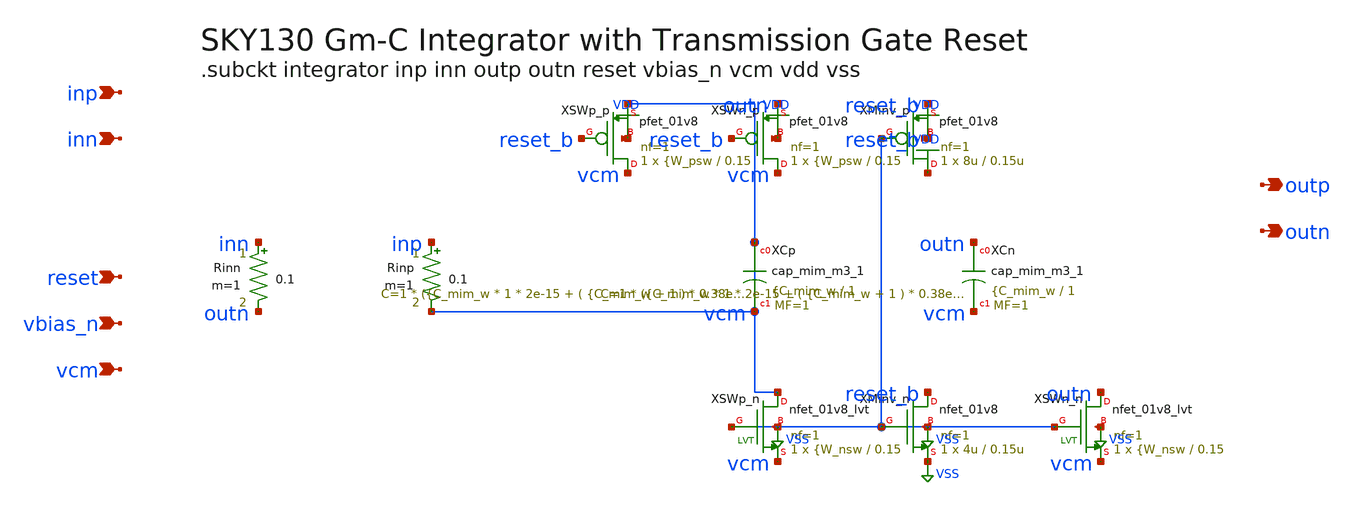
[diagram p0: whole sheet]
** sch_path: data/sch/ode_integrator.sch
**.subckt ode_integrator inp inn outp outn reset vbias_n vcm
*.ipin inp
*.ipin inn
*.opin outp
*.opin outn
*.ipin reset
*.ipin vbias_n
*.ipin vcm
XXMinv_n reset_b VSS VSS VSS sky130_fd_pr__nfet_01v8 L=0.15u W=4u nf=1 ad='int((1 + 1)/2) * 4u / 1 * 0.29'
+ as='int((1 + 2)/2) * 4u / 1 * 0.29' pd='2*int((1 + 1)/2) * (4u / 1 + 0.29)' ps='2*int((1 + 2)/2) * (4u / 1 + 0.29)'
+ nrd='0.29 / 4u ' nrs='0.29 / 4u ' sa=0 sb=0 sd=0 mult=1 m=1
XXMinv_p VDD VSS reset_b VDD sky130_fd_pr__pfet_01v8 L=0.15u W=8u nf=1 ad='int((nf+1)/2) * W/nf * 0.29'
+ as='int((nf+2)/2) * W/nf * 0.29' pd='2*int((nf+1)/2) * (W/nf + 0.29)' ps='2*int((nf+2)/2) * (W/nf + 0.29)'
+ nrd='0.29 / W' nrs='0.29 / W' sa=0 sb=0 sd=0 mult=1 m=1
XXCp vcm vcm sky130_fd_pr__cap_mim_m3_1 W={C_mim_w L=1 MF=1 m=1
XXSWp_n vcm VSS vcm VSS sky130_fd_pr__nfet_01v8_lvt L=0.15 W={W_nsw nf=1 ad='int((1 + 1)/2) * {W_nsw
+ / 1 * 0.29' as='int((1 + 2)/2) * {W_nsw / 1 * 0.29' pd='2*int((1 + 1)/2) * ({W_nsw / 1 + 0.29)' ps='2*int((1
+ + 2)/2) * ({W_nsw / 1 + 0.29)' nrd='0.29 / {W_nsw ' nrs='0.29 / {W_nsw ' sa=0 sb=0 sd=0 mult=1 m=1
XXSWp_p vcm reset_b vcm VDD sky130_fd_pr__pfet_01v8 L=0.15 W={W_psw nf=1 ad='int((nf+1)/2) * W/nf * 0.29' as='int((nf+2)/2)
+ * W/nf * 0.29' pd='2*int((nf+1)/2) * (W/nf + 0.29)' ps='2*int((nf+2)/2) * (W/nf + 0.29)' nrd='0.29 /
+ W' nrs='0.29 / W' sa=0 sb=0 sd=0 mult=1 m=1
XXCn outn vcm sky130_fd_pr__cap_mim_m3_1 W={C_mim_w L=1 MF=1 m=1
XXSWn_n outn VSS vcm VSS sky130_fd_pr__nfet_01v8_lvt L=0.15 W={W_nsw nf=1 ad='int((1 + 1)/2) * {W_nsw / 1 * 0.29'
+ as='int((1 + 2)/2) * {W_nsw / 1 * 0.29' pd='2*int((1 + 1)/2) * ({W_nsw / 1 + 0.29)' ps='2*int((1 + 2)/2) * ({W_nsw
+ / 1 + 0.29)' nrd='0.29 / {W_nsw ' nrs='0.29 / {W_nsw ' sa=0 sb=0 sd=0 mult=1 m=1
XXSWn_p vcm reset_b outn VDD sky130_fd_pr__pfet_01v8 L=0.15 W={W_psw nf=1 ad='int((nf+1)/2) * W/nf * 0.29'
+ as='int((nf+2)/2) * W/nf * 0.29' pd='2*int((nf+1)/2) * (W/nf + 0.29)' ps='2*int((nf+2)/2) * (W/nf + 0.29)'
+ nrd='0.29 / W' nrs='0.29 / W' sa=0 sb=0 sd=0 mult=1 m=1
Rinp inp vcm 0.1 m=1
Rinn inn outn 0.1 m=1
**.ends
.GLOBAL VSS
.GLOBAL VDD
.end
